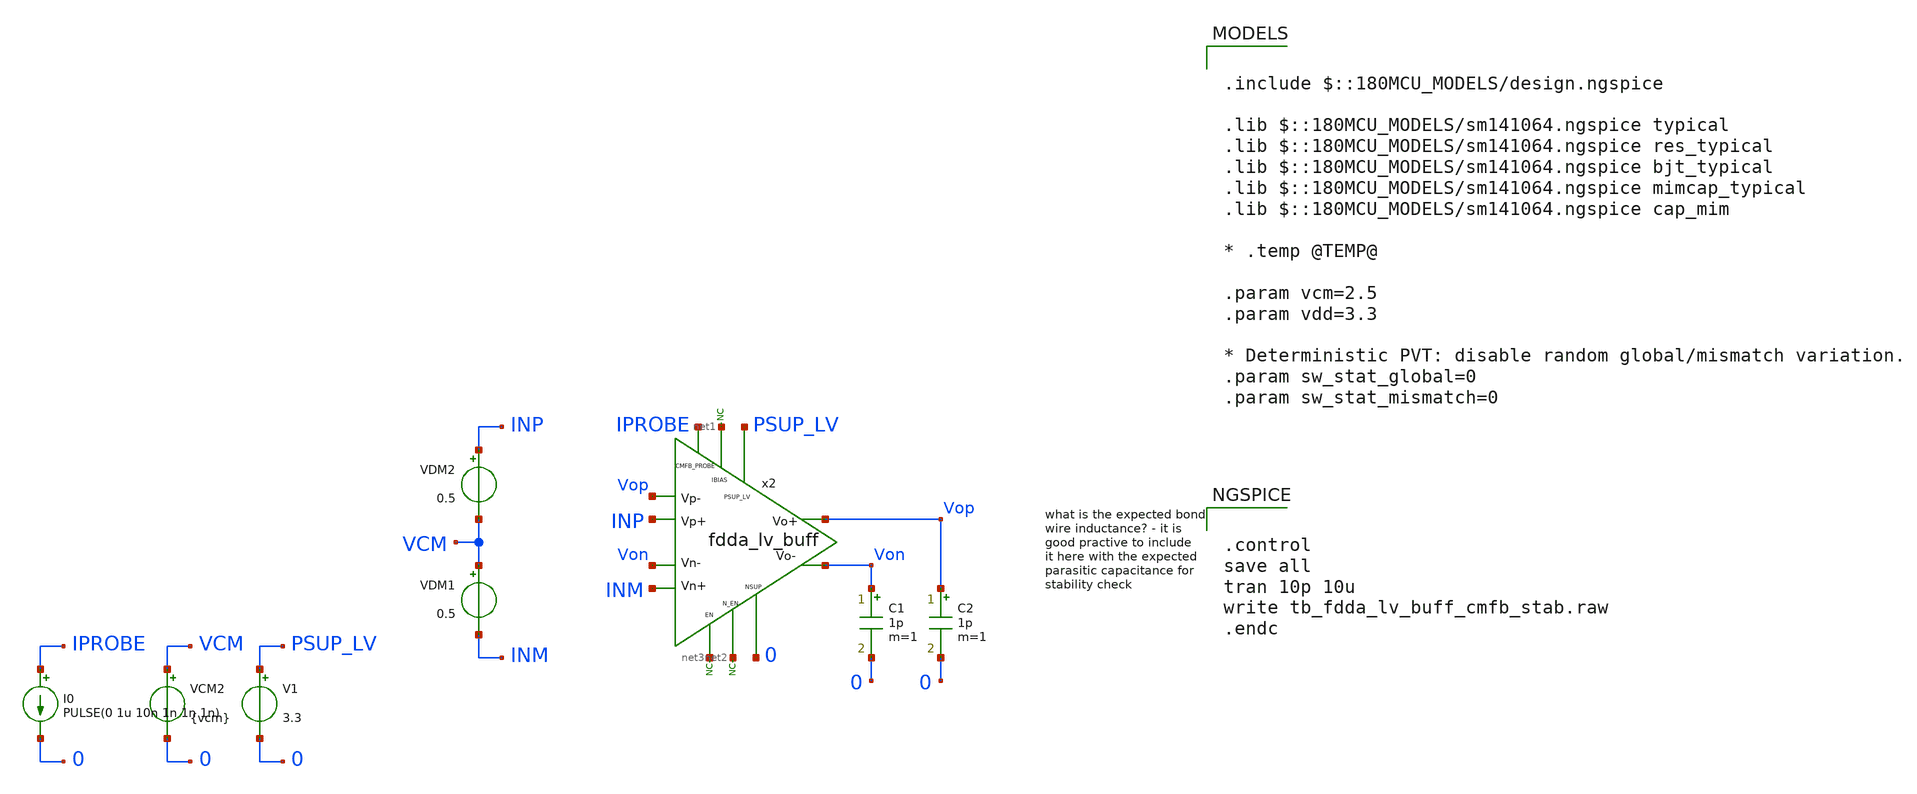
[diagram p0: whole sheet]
** sch_path: xschem/blocks/fdda_lv_buff/tb_fdda_lv_buff_cmfb_stab.sch
**.subckt tb_fdda_lv_buff_cmfb_stab
C1 Von 0 1p m=1
x2 PSUP_LV Vop Von INM INP Vop Von net1 net2 net3 0 IPROBE fdda_lv_buff
* noconn #net1
* noconn #net3
* noconn #net2
V1 PSUP_LV 0 3.3
C2 Vop 0 1p m=1
VCM2 VCM 0 {vcm}
VDM2 INP VCM 0.5
VDM1 VCM INM 0.5
I0 IPROBE 0 PULSE(0 1u 10n 1n 1n 1n)
**** begin user architecture code

.include $::180MCU_MODELS/design.ngspice

.lib $::180MCU_MODELS/sm141064.ngspice typical
.lib $::180MCU_MODELS/sm141064.ngspice res_typical
.lib $::180MCU_MODELS/sm141064.ngspice bjt_typical
.lib $::180MCU_MODELS/sm141064.ngspice mimcap_typical
.lib $::180MCU_MODELS/sm141064.ngspice cap_mim

* .temp @TEMP@

.param vcm=2.5
.param vdd=3.3

* Deterministic PVT: disable random global/mismatch variation.
.param sw_stat_global=0
.param sw_stat_mismatch=0



.control
save all
tran 10p 10u
write tb_fdda_lv_buff_cmfb_stab.raw
.endc


**** end user architecture code
**.ends
.end
